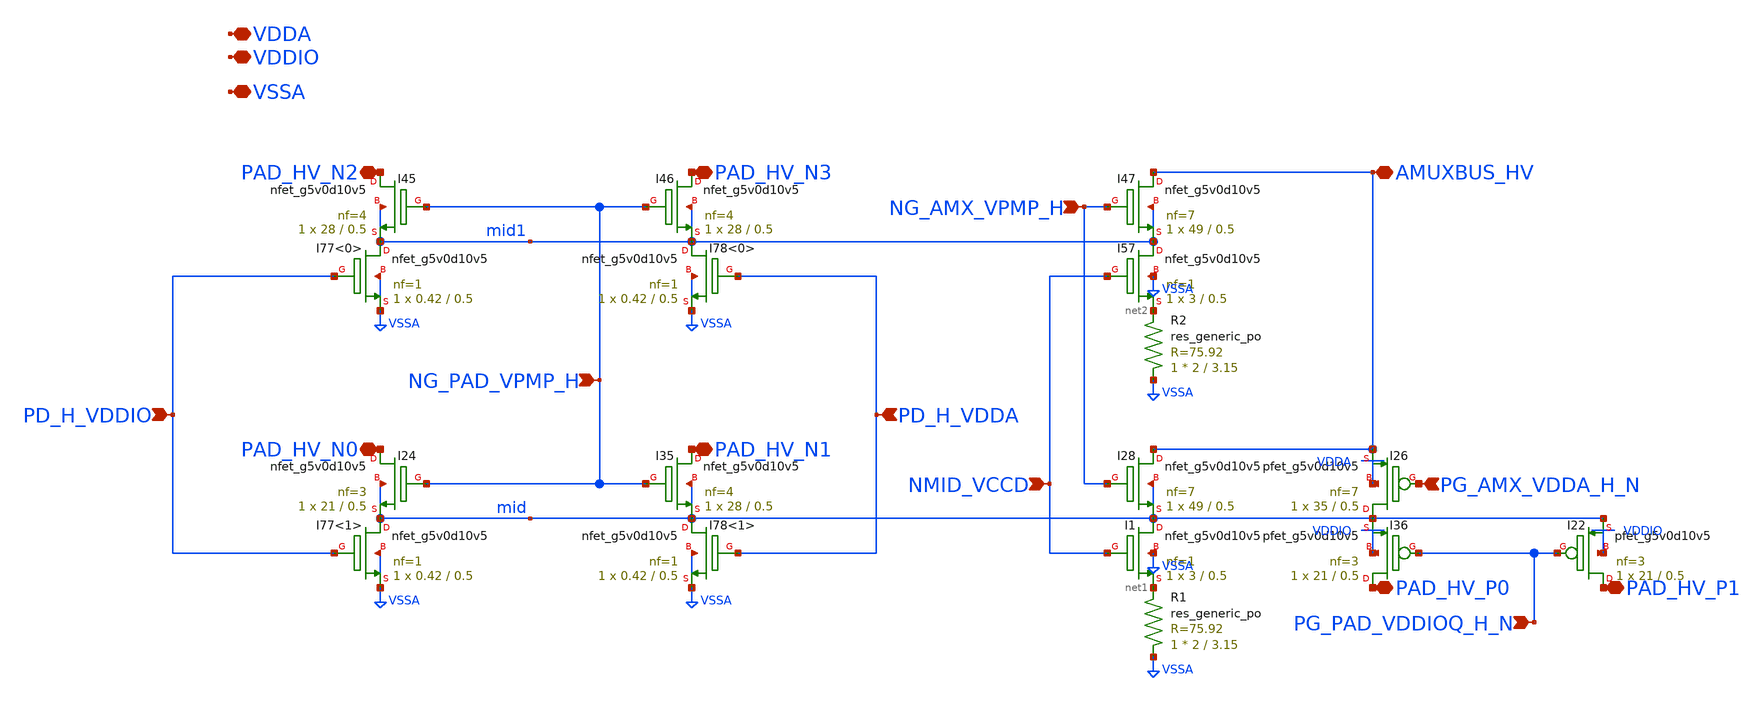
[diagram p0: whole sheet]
** sch_path: gpiov2_amux_switch.sch
* Copyright 2023 David Mitchell Bailey
* Licensed under the Apache License, Version 2.0 (the "License");
* you may not use this file except in compliance with the License.
* You may obtain a copy of the License at
* https://www.apache.org/licenses/LICENSE-2.0
* Unless required by applicable law or agreed to in writing, software
* distributed under the License is distributed on an "AS IS" BASIS,
* WITHOUT WARRANTIES OR CONDITIONS OF ANY KIND, either express or implied.
* See the License for the specific language governing permissions and
* limitations under the License.
**.subckt gpiov2_amux_switch PD_H_VDDA NMID_VCCD PG_AMX_VDDA_H_N PG_PAD_VDDIOQ_H_N AMUXBUS_HV
*+ PAD_HV_N1 PAD_HV_N0 PAD_HV_P0 PAD_HV_P1 NG_PAD_VPMP_H PD_H_VDDIO NG_AMX_VPMP_H PAD_HV_N3 PAD_HV_N2 VDDA VDDIO
*+ VSSA
*.ipin PD_H_VDDA
*.ipin NMID_VCCD
*.ipin PG_AMX_VDDA_H_N
*.ipin PG_PAD_VDDIOQ_H_N
*.iopin AMUXBUS_HV
*.iopin PAD_HV_N1
*.iopin PAD_HV_N0
*.iopin PAD_HV_P0
*.iopin PAD_HV_P1
*.ipin NG_PAD_VPMP_H
*.ipin PD_H_VDDIO
*.ipin NG_AMX_VPMP_H
*.iopin PAD_HV_N3
*.iopin PAD_HV_N2
*.iopin VDDA
*.iopin VDDIO
*.iopin VSSA
XI78<1> mid PD_H_VDDA VSSA VSSA sky130_fd_pr__nfet_g5v0d10v5 L=0.5 W=0.42 nf=1 ad='int((nf+1)/2) * W/nf * 0.29'
+ as='int((nf+2)/2) * W/nf * 0.29' pd='2*int((nf+1)/2) * (W/nf + 0.29)' ps='2*int((nf+2)/2) * (W/nf + 0.29)'
+ nrd='0.29 / W' nrs='0.29 / W' sa=0 sb=0 sd=0 mult=1 m=1
XI77<1> mid PD_H_VDDIO VSSA VSSA sky130_fd_pr__nfet_g5v0d10v5 L=0.5 W=0.42 nf=1 ad='int((nf+1)/2) * W/nf * 0.29'
+ as='int((nf+2)/2) * W/nf * 0.29' pd='2*int((nf+1)/2) * (W/nf + 0.29)' ps='2*int((nf+2)/2) * (W/nf + 0.29)'
+ nrd='0.29 / W' nrs='0.29 / W' sa=0 sb=0 sd=0 mult=1 m=1
XI24 PAD_HV_N0 NG_PAD_VPMP_H mid mid sky130_fd_pr__nfet_g5v0d10v5 L=0.5 W=21 nf=3 ad='int((nf+1)/2) * W/nf * 0.29'
+ as='int((nf+2)/2) * W/nf * 0.29' pd='2*int((nf+1)/2) * (W/nf + 0.29)' ps='2*int((nf+2)/2) * (W/nf + 0.29)'
+ nrd='0.29 / W' nrs='0.29 / W' sa=0 sb=0 sd=0 mult=1 m=1
XI35 PAD_HV_N1 NG_PAD_VPMP_H mid mid sky130_fd_pr__nfet_g5v0d10v5 L=0.5 W=28 nf=4 ad='int((nf+1)/2) * W/nf * 0.29'
+ as='int((nf+2)/2) * W/nf * 0.29' pd='2*int((nf+1)/2) * (W/nf + 0.29)' ps='2*int((nf+2)/2) * (W/nf + 0.29)'
+ nrd='0.29 / W' nrs='0.29 / W' sa=0 sb=0 sd=0 mult=1 m=1
XI28 AMUXBUS_HV NG_AMX_VPMP_H mid mid sky130_fd_pr__nfet_g5v0d10v5 L=0.5 W=49 nf=7 ad='int((nf+1)/2) * W/nf * 0.29'
+ as='int((nf+2)/2) * W/nf * 0.29' pd='2*int((nf+1)/2) * (W/nf + 0.29)' ps='2*int((nf+2)/2) * (W/nf + 0.29)'
+ nrd='0.29 / W' nrs='0.29 / W' sa=0 sb=0 sd=0 mult=1 m=1
XI36 PAD_HV_P0 PG_PAD_VDDIOQ_H_N mid VDDIO sky130_fd_pr__pfet_g5v0d10v5 L=0.5 W=21 nf=3 ad='int((nf+1)/2) * W/nf * 0.29'
+ as='int((nf+2)/2) * W/nf * 0.29' pd='2*int((nf+1)/2) * (W/nf + 0.29)' ps='2*int((nf+2)/2) * (W/nf + 0.29)'
+ nrd='0.29 / W' nrs='0.29 / W' sa=0 sb=0 sd=0 mult=1 m=1
XI22 PAD_HV_P1 PG_PAD_VDDIOQ_H_N mid VDDIO sky130_fd_pr__pfet_g5v0d10v5 L=0.5 W=21 nf=3 ad='int((nf+1)/2) * W/nf * 0.29'
+ as='int((nf+2)/2) * W/nf * 0.29' pd='2*int((nf+1)/2) * (W/nf + 0.29)' ps='2*int((nf+2)/2) * (W/nf + 0.29)'
+ nrd='0.29 / W' nrs='0.29 / W' sa=0 sb=0 sd=0 mult=1 m=1
XI1 mid NMID_VCCD net1 VSSA sky130_fd_pr__nfet_g5v0d10v5 L=0.5 W=3 nf=1 ad='int((nf+1)/2) * W/nf * 0.29'
+ as='int((nf+2)/2) * W/nf * 0.29' pd='2*int((nf+1)/2) * (W/nf + 0.29)' ps='2*int((nf+2)/2) * (W/nf + 0.29)'
+ nrd='0.29 / W' nrs='0.29 / W' sa=0 sb=0 sd=0 mult=1 m=1
XI26 mid PG_AMX_VDDA_H_N AMUXBUS_HV VDDA sky130_fd_pr__pfet_g5v0d10v5 L=0.5 W=35 nf=7 ad='int((nf+1)/2) * W/nf * 0.29'
+ as='int((nf+2)/2) * W/nf * 0.29' pd='2*int((nf+1)/2) * (W/nf + 0.29)' ps='2*int((nf+2)/2) * (W/nf + 0.29)'
+ nrd='0.29 / W' nrs='0.29 / W' sa=0 sb=0 sd=0 mult=1 m=1
XR1 VSSA net1 sky130_fd_pr__res_generic_po W=2 L=3.15 m=1
XI78<0> mid1 PD_H_VDDA VSSA VSSA sky130_fd_pr__nfet_g5v0d10v5 L=0.5 W=0.42 nf=1 ad='int((nf+1)/2) * W/nf * 0.29'
+ as='int((nf+2)/2) * W/nf * 0.29' pd='2*int((nf+1)/2) * (W/nf + 0.29)' ps='2*int((nf+2)/2) * (W/nf + 0.29)'
+ nrd='0.29 / W' nrs='0.29 / W' sa=0 sb=0 sd=0 mult=1 m=1
XI77<0> mid1 PD_H_VDDIO VSSA VSSA sky130_fd_pr__nfet_g5v0d10v5 L=0.5 W=0.42 nf=1 ad='int((nf+1)/2) * W/nf * 0.29'
+ as='int((nf+2)/2) * W/nf * 0.29' pd='2*int((nf+1)/2) * (W/nf + 0.29)' ps='2*int((nf+2)/2) * (W/nf + 0.29)'
+ nrd='0.29 / W' nrs='0.29 / W' sa=0 sb=0 sd=0 mult=1 m=1
XI45 PAD_HV_N2 NG_PAD_VPMP_H mid1 mid1 sky130_fd_pr__nfet_g5v0d10v5 L=0.5 W=28 nf=4 ad='int((nf+1)/2) * W/nf * 0.29'
+ as='int((nf+2)/2) * W/nf * 0.29' pd='2*int((nf+1)/2) * (W/nf + 0.29)' ps='2*int((nf+2)/2) * (W/nf + 0.29)'
+ nrd='0.29 / W' nrs='0.29 / W' sa=0 sb=0 sd=0 mult=1 m=1
XI46 PAD_HV_N3 NG_PAD_VPMP_H mid1 mid1 sky130_fd_pr__nfet_g5v0d10v5 L=0.5 W=28 nf=4 ad='int((nf+1)/2) * W/nf * 0.29'
+ as='int((nf+2)/2) * W/nf * 0.29' pd='2*int((nf+1)/2) * (W/nf + 0.29)' ps='2*int((nf+2)/2) * (W/nf + 0.29)'
+ nrd='0.29 / W' nrs='0.29 / W' sa=0 sb=0 sd=0 mult=1 m=1
XI47 AMUXBUS_HV NG_AMX_VPMP_H mid1 mid1 sky130_fd_pr__nfet_g5v0d10v5 L=0.5 W=49 nf=7 ad='int((nf+1)/2) * W/nf * 0.29'
+ as='int((nf+2)/2) * W/nf * 0.29' pd='2*int((nf+1)/2) * (W/nf + 0.29)' ps='2*int((nf+2)/2) * (W/nf + 0.29)'
+ nrd='0.29 / W' nrs='0.29 / W' sa=0 sb=0 sd=0 mult=1 m=1
XI57 mid1 NMID_VCCD net2 VSSA sky130_fd_pr__nfet_g5v0d10v5 L=0.5 W=3 nf=1 ad='int((nf+1)/2) * W/nf * 0.29'
+ as='int((nf+2)/2) * W/nf * 0.29' pd='2*int((nf+1)/2) * (W/nf + 0.29)' ps='2*int((nf+2)/2) * (W/nf + 0.29)'
+ nrd='0.29 / W' nrs='0.29 / W' sa=0 sb=0 sd=0 mult=1 m=1
XR2 VSSA net2 sky130_fd_pr__res_generic_po W=2 L=3.15 m=1
**.ends
.end
